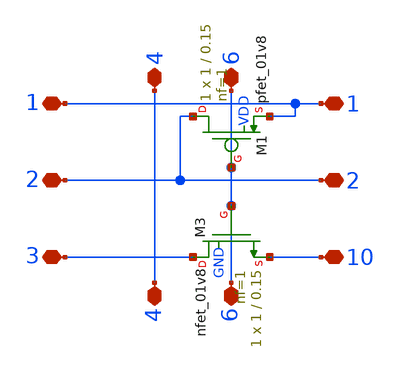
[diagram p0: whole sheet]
** sch_path: xschem/HW4_RAM_readout/new_cell.sch
**.subckt new_cell 3 2 1 4 6 10 2 1 4 6
*.iopin 3
*.iopin 2
*.iopin 1
*.iopin 4
*.iopin 6
*.iopin 10
*.iopin 2
*.iopin 1
*.iopin 4
*.iopin 6
XM3 3 6 10 GND sky130_fd_pr__nfet_01v8 L=0.15 W=1 nf=1 ad='int((nf+1)/2) * W/nf * 0.29' as='int((nf+2)/2) * W/nf * 0.29'
+ pd='2*int((nf+1)/2) * (W/nf + 0.29)' ps='2*int((nf+2)/2) * (W/nf + 0.29)' nrd='0.29 / W' nrs='0.29 / W'
+ sa=0 sb=0 sd=0 mult=1 m=1
XM1 2 6 1 VDD sky130_fd_pr__pfet_01v8 L=0.15 W=1 nf=1 ad='int((nf+1)/2) * W/nf * 0.29' as='int((nf+2)/2) * W/nf * 0.29'
+ pd='2*int((nf+1)/2) * (W/nf + 0.29)' ps='2*int((nf+2)/2) * (W/nf + 0.29)' nrd='0.29 / W' nrs='0.29 / W'
+ sa=0 sb=0 sd=0 mult=1 m=1
**.ends
.end
